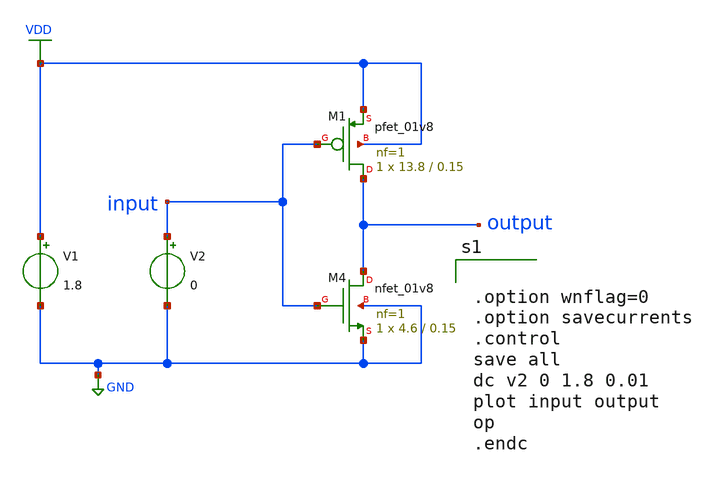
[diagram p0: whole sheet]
** sch_path: Schematic/Novaldy_5022211146.sch
**.subckt Novaldy_5022211146
V1 VDD GND 1.8
V2 input GND 0
XM1 output input VDD VDD sky130_fd_pr__pfet_01v8 L=0.15 W=13.8 nf=1 ad='int((nf+1)/2) * W/nf * 0.29'
+ as='int((nf+2)/2) * W/nf * 0.29' pd='2*int((nf+1)/2) * (W/nf + 0.29)' ps='2*int((nf+2)/2) * (W/nf + 0.29)'
+ nrd='0.29 / W' nrs='0.29 / W' sa=0 sb=0 sd=0 mult=1 m=1
XM4 output input GND GND sky130_fd_pr__nfet_01v8 L=0.15 W=4.6 nf=1 ad='int((nf+1)/2) * W/nf * 0.29' as='int((nf+2)/2) * W/nf * 0.29'
+ pd='2*int((nf+1)/2) * (W/nf + 0.29)' ps='2*int((nf+2)/2) * (W/nf + 0.29)' nrd='0.29 / W' nrs='0.29 / W'
+ sa=0 sb=0 sd=0 mult=1 m=1
**** begin user architecture code
 .lib $::SKYWATER_MODELS/sky130.lib.spice tt
.param mc_mmm_cwitch=0
.param mc_pr_switch=1



.option wnflag=0
.option savecurrents
.control
save all
dc v2 0 1.8 0.01
plot input output
op
.endc


**** end user architecture code
**.ends
.GLOBAL GND
.GLOBAL VDD
.end
